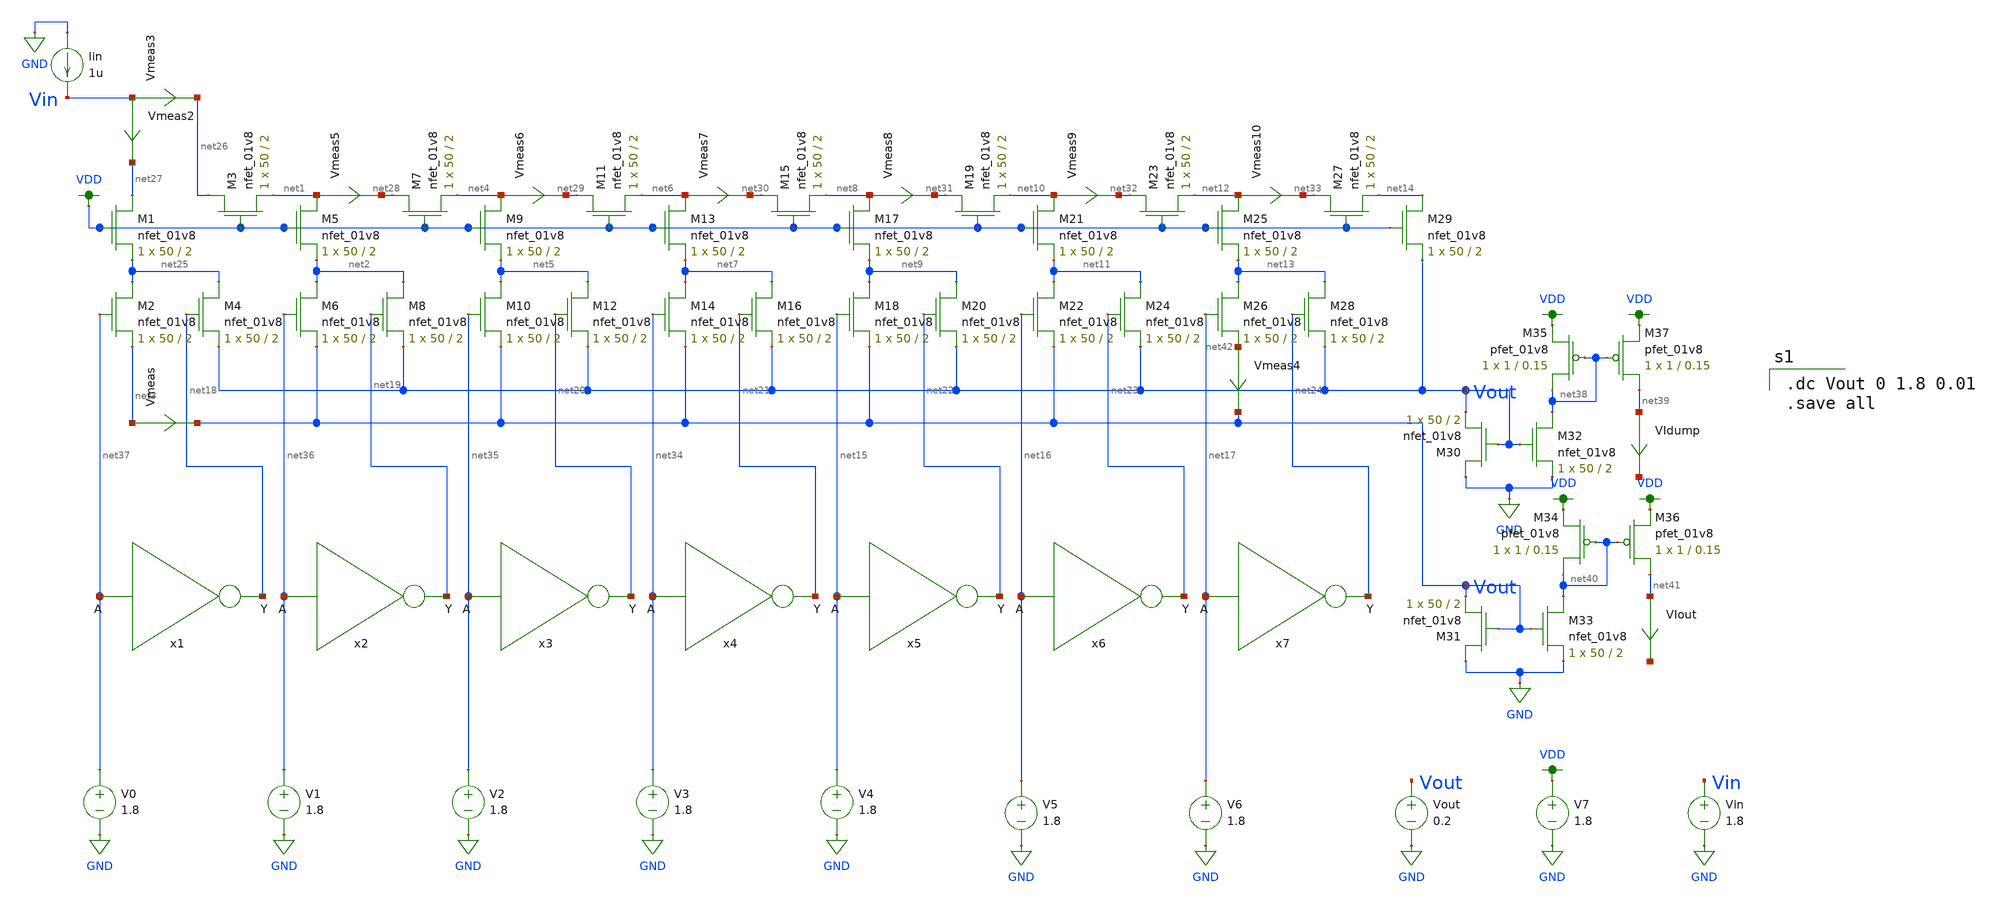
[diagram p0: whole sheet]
** sch_path: xschem/ladder_lauren.sch
**.subckt ladder_lauren
XM1 net27 VDD net25 GND sky130_fd_pr__nfet_01v8 L=2 W=50 nf=1 ad='int((nf+1)/2) * W/nf * 0.29' as='int((nf+2)/2) * W/nf * 0.29'
+ pd='2*int((nf+1)/2) * (W/nf + 0.29)' ps='2*int((nf+2)/2) * (W/nf + 0.29)' nrd='0.29 / W' nrs='0.29 / W'
+ sa=0 sb=0 sd=0 mult=1 m=1
XM3 net26 VDD net1 GND sky130_fd_pr__nfet_01v8 L=2 W=50 nf=1 ad='int((nf+1)/2) * W/nf * 0.29' as='int((nf+2)/2) * W/nf * 0.29'
+ pd='2*int((nf+1)/2) * (W/nf + 0.29)' ps='2*int((nf+2)/2) * (W/nf + 0.29)' nrd='0.29 / W' nrs='0.29 / W'
+ sa=0 sb=0 sd=0 mult=1 m=1
XM5 net1 VDD net2 GND sky130_fd_pr__nfet_01v8 L=2 W=50 nf=1 ad='int((nf+1)/2) * W/nf * 0.29' as='int((nf+2)/2) * W/nf * 0.29'
+ pd='2*int((nf+1)/2) * (W/nf + 0.29)' ps='2*int((nf+2)/2) * (W/nf + 0.29)' nrd='0.29 / W' nrs='0.29 / W'
+ sa=0 sb=0 sd=0 mult=1 m=1
XM7 net28 VDD net4 GND sky130_fd_pr__nfet_01v8 L=2 W=50 nf=1 ad='int((nf+1)/2) * W/nf * 0.29' as='int((nf+2)/2) * W/nf * 0.29'
+ pd='2*int((nf+1)/2) * (W/nf + 0.29)' ps='2*int((nf+2)/2) * (W/nf + 0.29)' nrd='0.29 / W' nrs='0.29 / W'
+ sa=0 sb=0 sd=0 mult=1 m=1
XM6 net2 net36 Vout GND sky130_fd_pr__nfet_01v8 L=2 W=50 nf=1 ad='int((nf+1)/2) * W/nf * 0.29' as='int((nf+2)/2) * W/nf * 0.29'
+ pd='2*int((nf+1)/2) * (W/nf + 0.29)' ps='2*int((nf+2)/2) * (W/nf + 0.29)' nrd='0.29 / W' nrs='0.29 / W'
+ sa=0 sb=0 sd=0 mult=1 m=1
XM8 net2 net19 Vout GND sky130_fd_pr__nfet_01v8 L=2 W=50 nf=1 ad='int((nf+1)/2) * W/nf * 0.29' as='int((nf+2)/2) * W/nf * 0.29'
+ pd='2*int((nf+1)/2) * (W/nf + 0.29)' ps='2*int((nf+2)/2) * (W/nf + 0.29)' nrd='0.29 / W' nrs='0.29 / W'
+ sa=0 sb=0 sd=0 mult=1 m=1
XM2 net25 net37 net3 GND sky130_fd_pr__nfet_01v8 L=2 W=50 nf=1 ad='int((nf+1)/2) * W/nf * 0.29' as='int((nf+2)/2) * W/nf * 0.29'
+ pd='2*int((nf+1)/2) * (W/nf + 0.29)' ps='2*int((nf+2)/2) * (W/nf + 0.29)' nrd='0.29 / W' nrs='0.29 / W'
+ sa=0 sb=0 sd=0 mult=1 m=1
XM4 net25 net18 Vout GND sky130_fd_pr__nfet_01v8 L=2 W=50 nf=1 ad='int((nf+1)/2) * W/nf * 0.29' as='int((nf+2)/2) * W/nf * 0.29'
+ pd='2*int((nf+1)/2) * (W/nf + 0.29)' ps='2*int((nf+2)/2) * (W/nf + 0.29)' nrd='0.29 / W' nrs='0.29 / W'
+ sa=0 sb=0 sd=0 mult=1 m=1
XM9 net4 VDD net5 GND sky130_fd_pr__nfet_01v8 L=2 W=50 nf=1 ad='int((nf+1)/2) * W/nf * 0.29' as='int((nf+2)/2) * W/nf * 0.29'
+ pd='2*int((nf+1)/2) * (W/nf + 0.29)' ps='2*int((nf+2)/2) * (W/nf + 0.29)' nrd='0.29 / W' nrs='0.29 / W'
+ sa=0 sb=0 sd=0 mult=1 m=1
XM11 net29 VDD net6 GND sky130_fd_pr__nfet_01v8 L=2 W=50 nf=1 ad='int((nf+1)/2) * W/nf * 0.29' as='int((nf+2)/2) * W/nf * 0.29'
+ pd='2*int((nf+1)/2) * (W/nf + 0.29)' ps='2*int((nf+2)/2) * (W/nf + 0.29)' nrd='0.29 / W' nrs='0.29 / W'
+ sa=0 sb=0 sd=0 mult=1 m=1
XM10 net5 net35 Vout GND sky130_fd_pr__nfet_01v8 L=2 W=50 nf=1 ad='int((nf+1)/2) * W/nf * 0.29' as='int((nf+2)/2) * W/nf * 0.29'
+ pd='2*int((nf+1)/2) * (W/nf + 0.29)' ps='2*int((nf+2)/2) * (W/nf + 0.29)' nrd='0.29 / W' nrs='0.29 / W'
+ sa=0 sb=0 sd=0 mult=1 m=1
XM12 net5 net20 Vout GND sky130_fd_pr__nfet_01v8 L=2 W=50 nf=1 ad='int((nf+1)/2) * W/nf * 0.29' as='int((nf+2)/2) * W/nf * 0.29'
+ pd='2*int((nf+1)/2) * (W/nf + 0.29)' ps='2*int((nf+2)/2) * (W/nf + 0.29)' nrd='0.29 / W' nrs='0.29 / W'
+ sa=0 sb=0 sd=0 mult=1 m=1
XM13 net6 VDD net7 GND sky130_fd_pr__nfet_01v8 L=2 W=50 nf=1 ad='int((nf+1)/2) * W/nf * 0.29' as='int((nf+2)/2) * W/nf * 0.29'
+ pd='2*int((nf+1)/2) * (W/nf + 0.29)' ps='2*int((nf+2)/2) * (W/nf + 0.29)' nrd='0.29 / W' nrs='0.29 / W'
+ sa=0 sb=0 sd=0 mult=1 m=1
XM15 net30 VDD net8 GND sky130_fd_pr__nfet_01v8 L=2 W=50 nf=1 ad='int((nf+1)/2) * W/nf * 0.29' as='int((nf+2)/2) * W/nf * 0.29'
+ pd='2*int((nf+1)/2) * (W/nf + 0.29)' ps='2*int((nf+2)/2) * (W/nf + 0.29)' nrd='0.29 / W' nrs='0.29 / W'
+ sa=0 sb=0 sd=0 mult=1 m=1
XM14 net7 net34 Vout GND sky130_fd_pr__nfet_01v8 L=2 W=50 nf=1 ad='int((nf+1)/2) * W/nf * 0.29' as='int((nf+2)/2) * W/nf * 0.29'
+ pd='2*int((nf+1)/2) * (W/nf + 0.29)' ps='2*int((nf+2)/2) * (W/nf + 0.29)' nrd='0.29 / W' nrs='0.29 / W'
+ sa=0 sb=0 sd=0 mult=1 m=1
XM16 net7 net21 Vout GND sky130_fd_pr__nfet_01v8 L=2 W=50 nf=1 ad='int((nf+1)/2) * W/nf * 0.29' as='int((nf+2)/2) * W/nf * 0.29'
+ pd='2*int((nf+1)/2) * (W/nf + 0.29)' ps='2*int((nf+2)/2) * (W/nf + 0.29)' nrd='0.29 / W' nrs='0.29 / W'
+ sa=0 sb=0 sd=0 mult=1 m=1
XM17 net8 VDD net9 GND sky130_fd_pr__nfet_01v8 L=2 W=50 nf=1 ad='int((nf+1)/2) * W/nf * 0.29' as='int((nf+2)/2) * W/nf * 0.29'
+ pd='2*int((nf+1)/2) * (W/nf + 0.29)' ps='2*int((nf+2)/2) * (W/nf + 0.29)' nrd='0.29 / W' nrs='0.29 / W'
+ sa=0 sb=0 sd=0 mult=1 m=1
XM19 net31 VDD net10 GND sky130_fd_pr__nfet_01v8 L=2 W=50 nf=1 ad='int((nf+1)/2) * W/nf * 0.29' as='int((nf+2)/2) * W/nf * 0.29'
+ pd='2*int((nf+1)/2) * (W/nf + 0.29)' ps='2*int((nf+2)/2) * (W/nf + 0.29)' nrd='0.29 / W' nrs='0.29 / W'
+ sa=0 sb=0 sd=0 mult=1 m=1
XM18 net9 net15 Vout GND sky130_fd_pr__nfet_01v8 L=2 W=50 nf=1 ad='int((nf+1)/2) * W/nf * 0.29' as='int((nf+2)/2) * W/nf * 0.29'
+ pd='2*int((nf+1)/2) * (W/nf + 0.29)' ps='2*int((nf+2)/2) * (W/nf + 0.29)' nrd='0.29 / W' nrs='0.29 / W'
+ sa=0 sb=0 sd=0 mult=1 m=1
XM20 net9 net22 Vout GND sky130_fd_pr__nfet_01v8 L=2 W=50 nf=1 ad='int((nf+1)/2) * W/nf * 0.29' as='int((nf+2)/2) * W/nf * 0.29'
+ pd='2*int((nf+1)/2) * (W/nf + 0.29)' ps='2*int((nf+2)/2) * (W/nf + 0.29)' nrd='0.29 / W' nrs='0.29 / W'
+ sa=0 sb=0 sd=0 mult=1 m=1
XM21 net10 VDD net11 GND sky130_fd_pr__nfet_01v8 L=2 W=50 nf=1 ad='int((nf+1)/2) * W/nf * 0.29' as='int((nf+2)/2) * W/nf * 0.29'
+ pd='2*int((nf+1)/2) * (W/nf + 0.29)' ps='2*int((nf+2)/2) * (W/nf + 0.29)' nrd='0.29 / W' nrs='0.29 / W'
+ sa=0 sb=0 sd=0 mult=1 m=1
XM23 net32 VDD net12 GND sky130_fd_pr__nfet_01v8 L=2 W=50 nf=1 ad='int((nf+1)/2) * W/nf * 0.29' as='int((nf+2)/2) * W/nf * 0.29'
+ pd='2*int((nf+1)/2) * (W/nf + 0.29)' ps='2*int((nf+2)/2) * (W/nf + 0.29)' nrd='0.29 / W' nrs='0.29 / W'
+ sa=0 sb=0 sd=0 mult=1 m=1
XM22 net11 net16 Vout GND sky130_fd_pr__nfet_01v8 L=2 W=50 nf=1 ad='int((nf+1)/2) * W/nf * 0.29' as='int((nf+2)/2) * W/nf * 0.29'
+ pd='2*int((nf+1)/2) * (W/nf + 0.29)' ps='2*int((nf+2)/2) * (W/nf + 0.29)' nrd='0.29 / W' nrs='0.29 / W'
+ sa=0 sb=0 sd=0 mult=1 m=1
XM24 net11 net23 Vout GND sky130_fd_pr__nfet_01v8 L=2 W=50 nf=1 ad='int((nf+1)/2) * W/nf * 0.29' as='int((nf+2)/2) * W/nf * 0.29'
+ pd='2*int((nf+1)/2) * (W/nf + 0.29)' ps='2*int((nf+2)/2) * (W/nf + 0.29)' nrd='0.29 / W' nrs='0.29 / W'
+ sa=0 sb=0 sd=0 mult=1 m=1
XM25 net12 VDD net13 GND sky130_fd_pr__nfet_01v8 L=2 W=50 nf=1 ad='int((nf+1)/2) * W/nf * 0.29' as='int((nf+2)/2) * W/nf * 0.29'
+ pd='2*int((nf+1)/2) * (W/nf + 0.29)' ps='2*int((nf+2)/2) * (W/nf + 0.29)' nrd='0.29 / W' nrs='0.29 / W'
+ sa=0 sb=0 sd=0 mult=1 m=1
XM27 net33 VDD net14 GND sky130_fd_pr__nfet_01v8 L=2 W=50 nf=1 ad='int((nf+1)/2) * W/nf * 0.29' as='int((nf+2)/2) * W/nf * 0.29'
+ pd='2*int((nf+1)/2) * (W/nf + 0.29)' ps='2*int((nf+2)/2) * (W/nf + 0.29)' nrd='0.29 / W' nrs='0.29 / W'
+ sa=0 sb=0 sd=0 mult=1 m=1
XM26 net13 net17 net42 GND sky130_fd_pr__nfet_01v8 L=2 W=50 nf=1 ad='int((nf+1)/2) * W/nf * 0.29' as='int((nf+2)/2) * W/nf * 0.29'
+ pd='2*int((nf+1)/2) * (W/nf + 0.29)' ps='2*int((nf+2)/2) * (W/nf + 0.29)' nrd='0.29 / W' nrs='0.29 / W'
+ sa=0 sb=0 sd=0 mult=1 m=1
XM28 net13 net24 Vout GND sky130_fd_pr__nfet_01v8 L=2 W=50 nf=1 ad='int((nf+1)/2) * W/nf * 0.29' as='int((nf+2)/2) * W/nf * 0.29'
+ pd='2*int((nf+1)/2) * (W/nf + 0.29)' ps='2*int((nf+2)/2) * (W/nf + 0.29)' nrd='0.29 / W' nrs='0.29 / W'
+ sa=0 sb=0 sd=0 mult=1 m=1
XM29 net14 VDD Vout GND sky130_fd_pr__nfet_01v8 L=2 W=50 nf=1 ad='int((nf+1)/2) * W/nf * 0.29' as='int((nf+2)/2) * W/nf * 0.29'
+ pd='2*int((nf+1)/2) * (W/nf + 0.29)' ps='2*int((nf+2)/2) * (W/nf + 0.29)' nrd='0.29 / W' nrs='0.29 / W'
+ sa=0 sb=0 sd=0 mult=1 m=1
XM30 GND Vout Vout GND sky130_fd_pr__nfet_01v8 L=2 W=50 nf=1 ad='int((nf+1)/2) * W/nf * 0.29' as='int((nf+2)/2) * W/nf * 0.29'
+ pd='2*int((nf+1)/2) * (W/nf + 0.29)' ps='2*int((nf+2)/2) * (W/nf + 0.29)' nrd='0.29 / W' nrs='0.29 / W'
+ sa=0 sb=0 sd=0 mult=1 m=1
XM31 GND Vout Vout GND sky130_fd_pr__nfet_01v8 L=2 W=50 nf=1 ad='int((nf+1)/2) * W/nf * 0.29' as='int((nf+2)/2) * W/nf * 0.29'
+ pd='2*int((nf+1)/2) * (W/nf + 0.29)' ps='2*int((nf+2)/2) * (W/nf + 0.29)' nrd='0.29 / W' nrs='0.29 / W'
+ sa=0 sb=0 sd=0 mult=1 m=1
XM32 net38 Vout GND GND sky130_fd_pr__nfet_01v8 L=2 W=50 nf=1 ad='int((nf+1)/2) * W/nf * 0.29' as='int((nf+2)/2) * W/nf * 0.29'
+ pd='2*int((nf+1)/2) * (W/nf + 0.29)' ps='2*int((nf+2)/2) * (W/nf + 0.29)' nrd='0.29 / W' nrs='0.29 / W'
+ sa=0 sb=0 sd=0 mult=1 m=1
XM33 net40 Vout GND GND sky130_fd_pr__nfet_01v8 L=2 W=50 nf=1 ad='int((nf+1)/2) * W/nf * 0.29' as='int((nf+2)/2) * W/nf * 0.29'
+ pd='2*int((nf+1)/2) * (W/nf + 0.29)' ps='2*int((nf+2)/2) * (W/nf + 0.29)' nrd='0.29 / W' nrs='0.29 / W'
+ sa=0 sb=0 sd=0 mult=1 m=1
x1 net18 net37 inverter
x2 net19 net36 inverter
x3 net20 net35 inverter
x4 net21 net34 inverter
x5 net22 net15 inverter
x6 net23 net16 inverter
x7 net24 net17 inverter
Iin GND Vin 1u
V0 net37 GND 1.8
V1 net36 GND 1.8
V2 net35 GND 1.8
V3 net34 GND 1.8
V4 net15 GND 1.8
V5 net16 GND 1.8
V6 net17 GND 1.8
VIout net41 net43 0
.save i(viout)
VIdump net39 net44 0
.save i(vidump)
Vout Vout GND 0.2
Vmeas net3 Vout 0
.save i(vmeas)
Vmeas3 Vin net26 0
.save i(vmeas3)
Vmeas4 net42 Vout 0
.save i(vmeas4)
Vmeas5 net1 net28 0
.save i(vmeas5)
Vmeas6 net4 net29 0
.save i(vmeas6)
Vmeas7 net6 net30 0
.save i(vmeas7)
Vin Vin GND 1.8
Vmeas2 Vin net27 0
.save i(vmeas2)
Vmeas8 net8 net31 0
.save i(vmeas8)
Vmeas9 net10 net32 0
.save i(vmeas9)
Vmeas10 net12 net33 0
.save i(vmeas10)
XM35 net38 net38 VDD VDD sky130_fd_pr__pfet_01v8 L=0.15 W=1 nf=1 ad='int((nf+1)/2) * W/nf * 0.29' as='int((nf+2)/2) * W/nf * 0.29'
+ pd='2*int((nf+1)/2) * (W/nf + 0.29)' ps='2*int((nf+2)/2) * (W/nf + 0.29)' nrd='0.29 / W' nrs='0.29 / W'
+ sa=0 sb=0 sd=0 mult=1 m=1
XM37 net39 net38 VDD VDD sky130_fd_pr__pfet_01v8 L=0.15 W=1 nf=1 ad='int((nf+1)/2) * W/nf * 0.29' as='int((nf+2)/2) * W/nf * 0.29'
+ pd='2*int((nf+1)/2) * (W/nf + 0.29)' ps='2*int((nf+2)/2) * (W/nf + 0.29)' nrd='0.29 / W' nrs='0.29 / W'
+ sa=0 sb=0 sd=0 mult=1 m=1
XM34 net40 net40 VDD VDD sky130_fd_pr__pfet_01v8 L=0.15 W=1 nf=1 ad='int((nf+1)/2) * W/nf * 0.29' as='int((nf+2)/2) * W/nf * 0.29'
+ pd='2*int((nf+1)/2) * (W/nf + 0.29)' ps='2*int((nf+2)/2) * (W/nf + 0.29)' nrd='0.29 / W' nrs='0.29 / W'
+ sa=0 sb=0 sd=0 mult=1 m=1
XM36 net41 net40 VDD VDD sky130_fd_pr__pfet_01v8 L=0.15 W=1 nf=1 ad='int((nf+1)/2) * W/nf * 0.29' as='int((nf+2)/2) * W/nf * 0.29'
+ pd='2*int((nf+1)/2) * (W/nf + 0.29)' ps='2*int((nf+2)/2) * (W/nf + 0.29)' nrd='0.29 / W' nrs='0.29 / W'
+ sa=0 sb=0 sd=0 mult=1 m=1
V7 VDD GND 1.8
**** begin user architecture code

.option wnflag=1
.lib ~/skywater/skywater-pdk/libraries/sky130_fd_pr_ngspice/latest/models/sky130.lib.spice tt


.dc Vout 0 1.8 0.01
.save all

**** end user architecture code
**.ends

* expanding   symbol:  ./inverter.sym # of pins=2
** sym_path: xschem/inverter.sym
** sch_path: xschem/inverter.sch
.subckt inverter Y A
*.ipin A
*.opin Y
XM1 Y A VDD VDD sky130_fd_pr__pfet_01v8 L=0.15 W=1 nf=1 ad='int((nf+1)/2) * W/nf * 0.29' as='int((nf+2)/2) * W/nf * 0.29'
+ pd='2*int((nf+1)/2) * (W/nf + 0.29)' ps='2*int((nf+2)/2) * (W/nf + 0.29)' nrd='0.29 / W' nrs='0.29 / W'
+ sa=0 sb=0 sd=0 mult=1 m=1
XM2 Y A GND GND sky130_fd_pr__nfet_01v8 L=0.15 W=1 nf=1 ad='int((nf+1)/2) * W/nf * 0.29' as='int((nf+2)/2) * W/nf * 0.29'
+ pd='2*int((nf+1)/2) * (W/nf + 0.29)' ps='2*int((nf+2)/2) * (W/nf + 0.29)' nrd='0.29 / W' nrs='0.29 / W'
+ sa=0 sb=0 sd=0 mult=1 m=1
.ends

.GLOBAL VDD
.GLOBAL GND
.end
